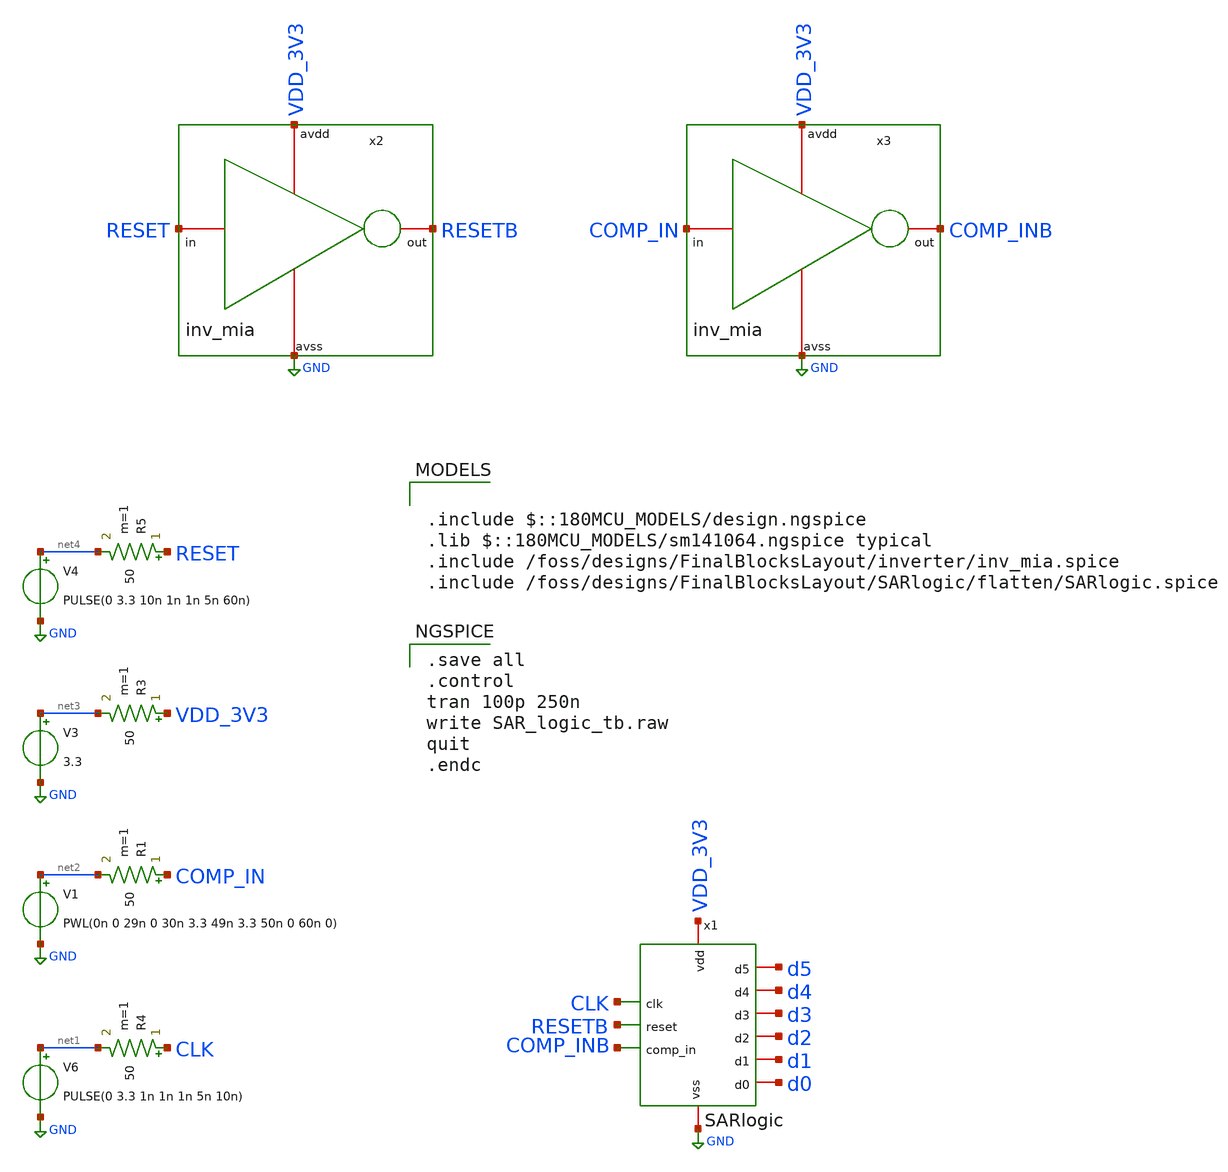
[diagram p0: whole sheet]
** sch_path: designs/FinalBlocksLayout/SARlogic/SAR_logic_tb.sch
**.subckt SAR_logic_tb
V6 net1 GND PULSE(0 3.3 1n 1n 1n 5n 10n)
R4 CLK net1 50 m=1
V1 net2 GND PWL(0n 0 29n 0 30n 3.3 49n 3.3 50n 0 60n 0)
R1 COMP_IN net2 50 m=1
V3 net3 GND 3.3
R3 VDD_3V3 net3 50 m=1
V4 net4 GND PULSE(0 3.3 10n 1n 1n 5n 60n)
R5 RESET net4 50 m=1
x2 VDD_3V3 RESET RESETB GND inv_mia
x3 VDD_3V3 COMP_IN COMP_INB GND inv_mia
x1 VDD_3V3 GND CLK RESETB COMP_INB d5 d4 d3 d2 d1 d0 SARlogic
**** begin user architecture code

.include $::180MCU_MODELS/design.ngspice
.lib $::180MCU_MODELS/sm141064.ngspice typical
.include /foss/designs/FinalBlocksLayout/inverter/inv_mia.spice
.include /foss/designs/FinalBlocksLayout/SARlogic/flatten/SARlogic.spice


.save all
.control
tran 100p 250n
write SAR_logic_tb.raw
quit
.endc

**** end user architecture code
**.ends
.GLOBAL GND
.end
